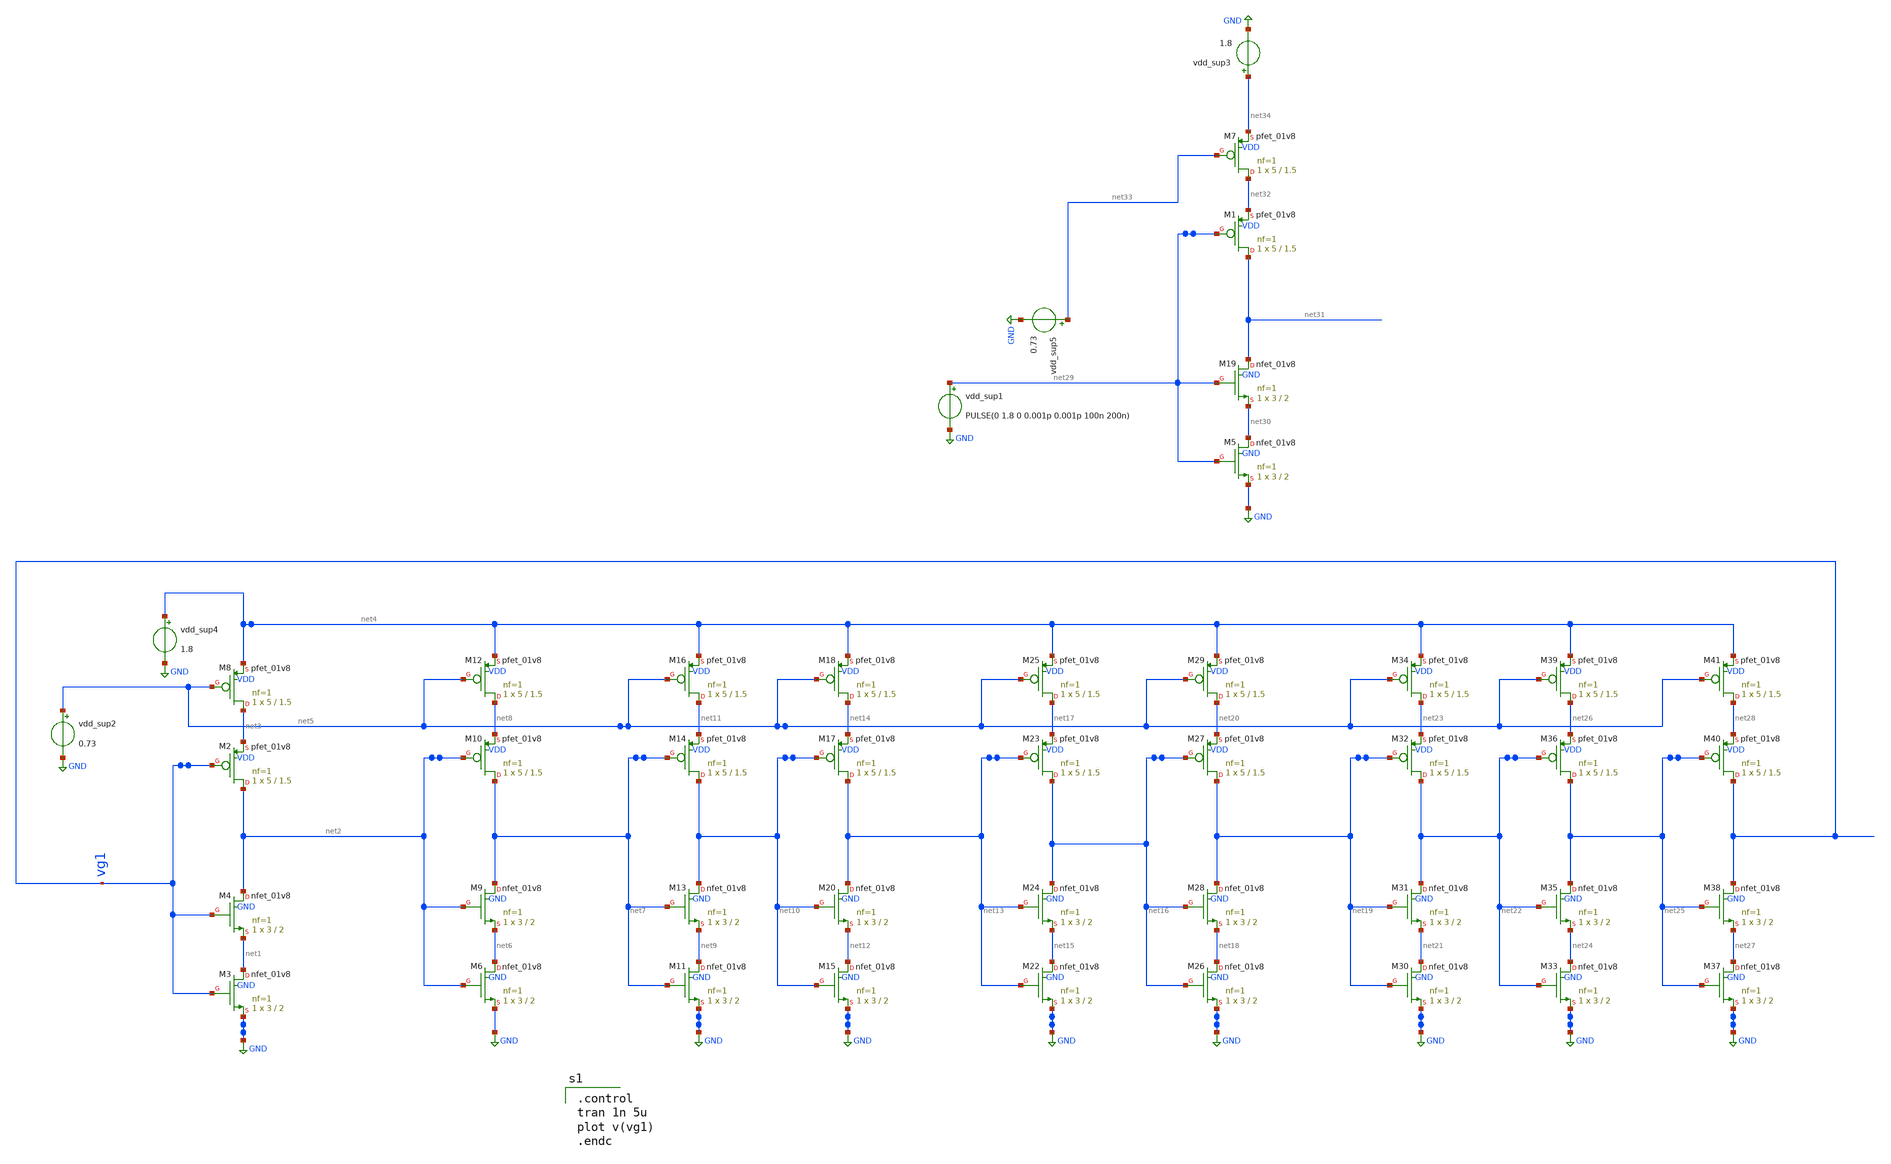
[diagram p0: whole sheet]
** sch_path: ring_osc_28_09.sch
**.subckt ring_osc_28_09
XM2 net2 vg1 net3 VDD sky130_fd_pr__pfet_01v8 L=1.5 W=5 nf=1 ad='int((nf+1)/2) * W/nf * 0.29' as='int((nf+2)/2) * W/nf * 0.29'
+ pd='2*int((nf+1)/2) * (W/nf + 0.29)' ps='2*int((nf+2)/2) * (W/nf + 0.29)' nrd='0.29 / W' nrs='0.29 / W'
+ sa=0 sb=0 sd=0 mult=1 m=1
XM3 net1 vg1 GND GND sky130_fd_pr__nfet_01v8 L=2 W=3 nf=1 ad='int((nf+1)/2) * W/nf * 0.29' as='int((nf+2)/2) * W/nf * 0.29'
+ pd='2*int((nf+1)/2) * (W/nf + 0.29)' ps='2*int((nf+2)/2) * (W/nf + 0.29)' nrd='0.29 / W' nrs='0.29 / W'
+ sa=0 sb=0 sd=0 mult=1 m=1
XM8 net3 net5 net4 VDD sky130_fd_pr__pfet_01v8 L=1.5 W=5 nf=1 ad='int((nf+1)/2) * W/nf * 0.29' as='int((nf+2)/2) * W/nf * 0.29'
+ pd='2*int((nf+1)/2) * (W/nf + 0.29)' ps='2*int((nf+2)/2) * (W/nf + 0.29)' nrd='0.29 / W' nrs='0.29 / W'
+ sa=0 sb=0 sd=0 mult=1 m=1
XM4 net2 vg1 net1 GND sky130_fd_pr__nfet_01v8 L=2 W=3 nf=1 ad='int((nf+1)/2) * W/nf * 0.29' as='int((nf+2)/2) * W/nf * 0.29'
+ pd='2*int((nf+1)/2) * (W/nf + 0.29)' ps='2*int((nf+2)/2) * (W/nf + 0.29)' nrd='0.29 / W' nrs='0.29 / W'
+ sa=0 sb=0 sd=0 mult=1 m=1
vdd_sup2 net5 GND 0.73
XM10 net7 net2 net8 VDD sky130_fd_pr__pfet_01v8 L=1.5 W=5 nf=1 ad='int((nf+1)/2) * W/nf * 0.29' as='int((nf+2)/2) * W/nf * 0.29'
+ pd='2*int((nf+1)/2) * (W/nf + 0.29)' ps='2*int((nf+2)/2) * (W/nf + 0.29)' nrd='0.29 / W' nrs='0.29 / W'
+ sa=0 sb=0 sd=0 mult=1 m=1
XM6 net6 net2 GND GND sky130_fd_pr__nfet_01v8 L=2 W=3 nf=1 ad='int((nf+1)/2) * W/nf * 0.29' as='int((nf+2)/2) * W/nf * 0.29'
+ pd='2*int((nf+1)/2) * (W/nf + 0.29)' ps='2*int((nf+2)/2) * (W/nf + 0.29)' nrd='0.29 / W' nrs='0.29 / W'
+ sa=0 sb=0 sd=0 mult=1 m=1
XM12 net8 net5 net4 VDD sky130_fd_pr__pfet_01v8 L=1.5 W=5 nf=1 ad='int((nf+1)/2) * W/nf * 0.29' as='int((nf+2)/2) * W/nf * 0.29'
+ pd='2*int((nf+1)/2) * (W/nf + 0.29)' ps='2*int((nf+2)/2) * (W/nf + 0.29)' nrd='0.29 / W' nrs='0.29 / W'
+ sa=0 sb=0 sd=0 mult=1 m=1
XM9 net7 net2 net6 GND sky130_fd_pr__nfet_01v8 L=2 W=3 nf=1 ad='int((nf+1)/2) * W/nf * 0.29' as='int((nf+2)/2) * W/nf * 0.29'
+ pd='2*int((nf+1)/2) * (W/nf + 0.29)' ps='2*int((nf+2)/2) * (W/nf + 0.29)' nrd='0.29 / W' nrs='0.29 / W'
+ sa=0 sb=0 sd=0 mult=1 m=1
XM14 net10 net7 net11 VDD sky130_fd_pr__pfet_01v8 L=1.5 W=5 nf=1 ad='int((nf+1)/2) * W/nf * 0.29' as='int((nf+2)/2) * W/nf * 0.29'
+ pd='2*int((nf+1)/2) * (W/nf + 0.29)' ps='2*int((nf+2)/2) * (W/nf + 0.29)' nrd='0.29 / W' nrs='0.29 / W'
+ sa=0 sb=0 sd=0 mult=1 m=1
XM11 net9 net7 GND GND sky130_fd_pr__nfet_01v8 L=2 W=3 nf=1 ad='int((nf+1)/2) * W/nf * 0.29' as='int((nf+2)/2) * W/nf * 0.29'
+ pd='2*int((nf+1)/2) * (W/nf + 0.29)' ps='2*int((nf+2)/2) * (W/nf + 0.29)' nrd='0.29 / W' nrs='0.29 / W'
+ sa=0 sb=0 sd=0 mult=1 m=1
XM16 net11 net5 net4 VDD sky130_fd_pr__pfet_01v8 L=1.5 W=5 nf=1 ad='int((nf+1)/2) * W/nf * 0.29' as='int((nf+2)/2) * W/nf * 0.29'
+ pd='2*int((nf+1)/2) * (W/nf + 0.29)' ps='2*int((nf+2)/2) * (W/nf + 0.29)' nrd='0.29 / W' nrs='0.29 / W'
+ sa=0 sb=0 sd=0 mult=1 m=1
XM13 net10 net7 net9 GND sky130_fd_pr__nfet_01v8 L=2 W=3 nf=1 ad='int((nf+1)/2) * W/nf * 0.29' as='int((nf+2)/2) * W/nf * 0.29'
+ pd='2*int((nf+1)/2) * (W/nf + 0.29)' ps='2*int((nf+2)/2) * (W/nf + 0.29)' nrd='0.29 / W' nrs='0.29 / W'
+ sa=0 sb=0 sd=0 mult=1 m=1
vdd_sup4 net4 GND 1.8
XM17 net13 net10 net14 VDD sky130_fd_pr__pfet_01v8 L=1.5 W=5 nf=1 ad='int((nf+1)/2) * W/nf * 0.29' as='int((nf+2)/2) * W/nf * 0.29'
+ pd='2*int((nf+1)/2) * (W/nf + 0.29)' ps='2*int((nf+2)/2) * (W/nf + 0.29)' nrd='0.29 / W' nrs='0.29 / W'
+ sa=0 sb=0 sd=0 mult=1 m=1
XM15 net12 net10 GND GND sky130_fd_pr__nfet_01v8 L=2 W=3 nf=1 ad='int((nf+1)/2) * W/nf * 0.29' as='int((nf+2)/2) * W/nf * 0.29'
+ pd='2*int((nf+1)/2) * (W/nf + 0.29)' ps='2*int((nf+2)/2) * (W/nf + 0.29)' nrd='0.29 / W' nrs='0.29 / W'
+ sa=0 sb=0 sd=0 mult=1 m=1
XM18 net14 net5 net4 VDD sky130_fd_pr__pfet_01v8 L=1.5 W=5 nf=1 ad='int((nf+1)/2) * W/nf * 0.29' as='int((nf+2)/2) * W/nf * 0.29'
+ pd='2*int((nf+1)/2) * (W/nf + 0.29)' ps='2*int((nf+2)/2) * (W/nf + 0.29)' nrd='0.29 / W' nrs='0.29 / W'
+ sa=0 sb=0 sd=0 mult=1 m=1
XM20 net13 net10 net12 GND sky130_fd_pr__nfet_01v8 L=2 W=3 nf=1 ad='int((nf+1)/2) * W/nf * 0.29' as='int((nf+2)/2) * W/nf * 0.29'
+ pd='2*int((nf+1)/2) * (W/nf + 0.29)' ps='2*int((nf+2)/2) * (W/nf + 0.29)' nrd='0.29 / W' nrs='0.29 / W'
+ sa=0 sb=0 sd=0 mult=1 m=1
XM23 net16 net13 net17 VDD sky130_fd_pr__pfet_01v8 L=1.5 W=5 nf=1 ad='int((nf+1)/2) * W/nf * 0.29' as='int((nf+2)/2) * W/nf * 0.29'
+ pd='2*int((nf+1)/2) * (W/nf + 0.29)' ps='2*int((nf+2)/2) * (W/nf + 0.29)' nrd='0.29 / W' nrs='0.29 / W'
+ sa=0 sb=0 sd=0 mult=1 m=1
XM22 net15 net13 GND GND sky130_fd_pr__nfet_01v8 L=2 W=3 nf=1 ad='int((nf+1)/2) * W/nf * 0.29' as='int((nf+2)/2) * W/nf * 0.29'
+ pd='2*int((nf+1)/2) * (W/nf + 0.29)' ps='2*int((nf+2)/2) * (W/nf + 0.29)' nrd='0.29 / W' nrs='0.29 / W'
+ sa=0 sb=0 sd=0 mult=1 m=1
XM25 net17 net5 net4 VDD sky130_fd_pr__pfet_01v8 L=1.5 W=5 nf=1 ad='int((nf+1)/2) * W/nf * 0.29' as='int((nf+2)/2) * W/nf * 0.29'
+ pd='2*int((nf+1)/2) * (W/nf + 0.29)' ps='2*int((nf+2)/2) * (W/nf + 0.29)' nrd='0.29 / W' nrs='0.29 / W'
+ sa=0 sb=0 sd=0 mult=1 m=1
XM24 net16 net13 net15 GND sky130_fd_pr__nfet_01v8 L=2 W=3 nf=1 ad='int((nf+1)/2) * W/nf * 0.29' as='int((nf+2)/2) * W/nf * 0.29'
+ pd='2*int((nf+1)/2) * (W/nf + 0.29)' ps='2*int((nf+2)/2) * (W/nf + 0.29)' nrd='0.29 / W' nrs='0.29 / W'
+ sa=0 sb=0 sd=0 mult=1 m=1
XM27 net19 net16 net20 VDD sky130_fd_pr__pfet_01v8 L=1.5 W=5 nf=1 ad='int((nf+1)/2) * W/nf * 0.29' as='int((nf+2)/2) * W/nf * 0.29'
+ pd='2*int((nf+1)/2) * (W/nf + 0.29)' ps='2*int((nf+2)/2) * (W/nf + 0.29)' nrd='0.29 / W' nrs='0.29 / W'
+ sa=0 sb=0 sd=0 mult=1 m=1
XM26 net18 net16 GND GND sky130_fd_pr__nfet_01v8 L=2 W=3 nf=1 ad='int((nf+1)/2) * W/nf * 0.29' as='int((nf+2)/2) * W/nf * 0.29'
+ pd='2*int((nf+1)/2) * (W/nf + 0.29)' ps='2*int((nf+2)/2) * (W/nf + 0.29)' nrd='0.29 / W' nrs='0.29 / W'
+ sa=0 sb=0 sd=0 mult=1 m=1
XM29 net20 net5 net4 VDD sky130_fd_pr__pfet_01v8 L=1.5 W=5 nf=1 ad='int((nf+1)/2) * W/nf * 0.29' as='int((nf+2)/2) * W/nf * 0.29'
+ pd='2*int((nf+1)/2) * (W/nf + 0.29)' ps='2*int((nf+2)/2) * (W/nf + 0.29)' nrd='0.29 / W' nrs='0.29 / W'
+ sa=0 sb=0 sd=0 mult=1 m=1
XM28 net19 net16 net18 GND sky130_fd_pr__nfet_01v8 L=2 W=3 nf=1 ad='int((nf+1)/2) * W/nf * 0.29' as='int((nf+2)/2) * W/nf * 0.29'
+ pd='2*int((nf+1)/2) * (W/nf + 0.29)' ps='2*int((nf+2)/2) * (W/nf + 0.29)' nrd='0.29 / W' nrs='0.29 / W'
+ sa=0 sb=0 sd=0 mult=1 m=1
XM32 net22 net19 net23 VDD sky130_fd_pr__pfet_01v8 L=1.5 W=5 nf=1 ad='int((nf+1)/2) * W/nf * 0.29' as='int((nf+2)/2) * W/nf * 0.29'
+ pd='2*int((nf+1)/2) * (W/nf + 0.29)' ps='2*int((nf+2)/2) * (W/nf + 0.29)' nrd='0.29 / W' nrs='0.29 / W'
+ sa=0 sb=0 sd=0 mult=1 m=1
XM30 net21 net19 GND GND sky130_fd_pr__nfet_01v8 L=2 W=3 nf=1 ad='int((nf+1)/2) * W/nf * 0.29' as='int((nf+2)/2) * W/nf * 0.29'
+ pd='2*int((nf+1)/2) * (W/nf + 0.29)' ps='2*int((nf+2)/2) * (W/nf + 0.29)' nrd='0.29 / W' nrs='0.29 / W'
+ sa=0 sb=0 sd=0 mult=1 m=1
XM34 net23 net5 net4 VDD sky130_fd_pr__pfet_01v8 L=1.5 W=5 nf=1 ad='int((nf+1)/2) * W/nf * 0.29' as='int((nf+2)/2) * W/nf * 0.29'
+ pd='2*int((nf+1)/2) * (W/nf + 0.29)' ps='2*int((nf+2)/2) * (W/nf + 0.29)' nrd='0.29 / W' nrs='0.29 / W'
+ sa=0 sb=0 sd=0 mult=1 m=1
XM31 net22 net19 net21 GND sky130_fd_pr__nfet_01v8 L=2 W=3 nf=1 ad='int((nf+1)/2) * W/nf * 0.29' as='int((nf+2)/2) * W/nf * 0.29'
+ pd='2*int((nf+1)/2) * (W/nf + 0.29)' ps='2*int((nf+2)/2) * (W/nf + 0.29)' nrd='0.29 / W' nrs='0.29 / W'
+ sa=0 sb=0 sd=0 mult=1 m=1
XM36 net25 net22 net26 VDD sky130_fd_pr__pfet_01v8 L=1.5 W=5 nf=1 ad='int((nf+1)/2) * W/nf * 0.29' as='int((nf+2)/2) * W/nf * 0.29'
+ pd='2*int((nf+1)/2) * (W/nf + 0.29)' ps='2*int((nf+2)/2) * (W/nf + 0.29)' nrd='0.29 / W' nrs='0.29 / W'
+ sa=0 sb=0 sd=0 mult=1 m=1
XM33 net24 net22 GND GND sky130_fd_pr__nfet_01v8 L=2 W=3 nf=1 ad='int((nf+1)/2) * W/nf * 0.29' as='int((nf+2)/2) * W/nf * 0.29'
+ pd='2*int((nf+1)/2) * (W/nf + 0.29)' ps='2*int((nf+2)/2) * (W/nf + 0.29)' nrd='0.29 / W' nrs='0.29 / W'
+ sa=0 sb=0 sd=0 mult=1 m=1
XM39 net26 net5 net4 VDD sky130_fd_pr__pfet_01v8 L=1.5 W=5 nf=1 ad='int((nf+1)/2) * W/nf * 0.29' as='int((nf+2)/2) * W/nf * 0.29'
+ pd='2*int((nf+1)/2) * (W/nf + 0.29)' ps='2*int((nf+2)/2) * (W/nf + 0.29)' nrd='0.29 / W' nrs='0.29 / W'
+ sa=0 sb=0 sd=0 mult=1 m=1
XM35 net25 net22 net24 GND sky130_fd_pr__nfet_01v8 L=2 W=3 nf=1 ad='int((nf+1)/2) * W/nf * 0.29' as='int((nf+2)/2) * W/nf * 0.29'
+ pd='2*int((nf+1)/2) * (W/nf + 0.29)' ps='2*int((nf+2)/2) * (W/nf + 0.29)' nrd='0.29 / W' nrs='0.29 / W'
+ sa=0 sb=0 sd=0 mult=1 m=1
XM40 vg1 net25 net28 VDD sky130_fd_pr__pfet_01v8 L=1.5 W=5 nf=1 ad='int((nf+1)/2) * W/nf * 0.29' as='int((nf+2)/2) * W/nf * 0.29'
+ pd='2*int((nf+1)/2) * (W/nf + 0.29)' ps='2*int((nf+2)/2) * (W/nf + 0.29)' nrd='0.29 / W' nrs='0.29 / W'
+ sa=0 sb=0 sd=0 mult=1 m=1
XM37 net27 net25 GND GND sky130_fd_pr__nfet_01v8 L=2 W=3 nf=1 ad='int((nf+1)/2) * W/nf * 0.29' as='int((nf+2)/2) * W/nf * 0.29'
+ pd='2*int((nf+1)/2) * (W/nf + 0.29)' ps='2*int((nf+2)/2) * (W/nf + 0.29)' nrd='0.29 / W' nrs='0.29 / W'
+ sa=0 sb=0 sd=0 mult=1 m=1
XM41 net28 net5 net4 VDD sky130_fd_pr__pfet_01v8 L=1.5 W=5 nf=1 ad='int((nf+1)/2) * W/nf * 0.29' as='int((nf+2)/2) * W/nf * 0.29'
+ pd='2*int((nf+1)/2) * (W/nf + 0.29)' ps='2*int((nf+2)/2) * (W/nf + 0.29)' nrd='0.29 / W' nrs='0.29 / W'
+ sa=0 sb=0 sd=0 mult=1 m=1
XM38 vg1 net25 net27 GND sky130_fd_pr__nfet_01v8 L=2 W=3 nf=1 ad='int((nf+1)/2) * W/nf * 0.29' as='int((nf+2)/2) * W/nf * 0.29'
+ pd='2*int((nf+1)/2) * (W/nf + 0.29)' ps='2*int((nf+2)/2) * (W/nf + 0.29)' nrd='0.29 / W' nrs='0.29 / W'
+ sa=0 sb=0 sd=0 mult=1 m=1
XM1 net31 net29 net32 VDD sky130_fd_pr__pfet_01v8 L=1.5 W=5 nf=1 ad='int((nf+1)/2) * W/nf * 0.29' as='int((nf+2)/2) * W/nf * 0.29'
+ pd='2*int((nf+1)/2) * (W/nf + 0.29)' ps='2*int((nf+2)/2) * (W/nf + 0.29)' nrd='0.29 / W' nrs='0.29 / W'
+ sa=0 sb=0 sd=0 mult=1 m=1
XM5 net30 net29 GND GND sky130_fd_pr__nfet_01v8 L=2 W=3 nf=1 ad='int((nf+1)/2) * W/nf * 0.29' as='int((nf+2)/2) * W/nf * 0.29'
+ pd='2*int((nf+1)/2) * (W/nf + 0.29)' ps='2*int((nf+2)/2) * (W/nf + 0.29)' nrd='0.29 / W' nrs='0.29 / W'
+ sa=0 sb=0 sd=0 mult=1 m=1
XM7 net32 net33 net34 VDD sky130_fd_pr__pfet_01v8 L=1.5 W=5 nf=1 ad='int((nf+1)/2) * W/nf * 0.29' as='int((nf+2)/2) * W/nf * 0.29'
+ pd='2*int((nf+1)/2) * (W/nf + 0.29)' ps='2*int((nf+2)/2) * (W/nf + 0.29)' nrd='0.29 / W' nrs='0.29 / W'
+ sa=0 sb=0 sd=0 mult=1 m=1
XM19 net31 net29 net30 GND sky130_fd_pr__nfet_01v8 L=2 W=3 nf=1 ad='int((nf+1)/2) * W/nf * 0.29' as='int((nf+2)/2) * W/nf * 0.29'
+ pd='2*int((nf+1)/2) * (W/nf + 0.29)' ps='2*int((nf+2)/2) * (W/nf + 0.29)' nrd='0.29 / W' nrs='0.29 / W'
+ sa=0 sb=0 sd=0 mult=1 m=1
vdd_sup1 net29 GND PULSE(0 1.8 0 0.001p 0.001p 100n 200n)
vdd_sup3 net34 GND 1.8
vdd_sup5 net33 GND 0.73
**** begin user architecture code


.lib /home/cegrahul/open_pdks/sky130/sky130A/libs.tech/ngspice/sky130.lib.spice tt
.MODEL swmod SW(VT=0.0 VH=0.01 RON=1 ROFF=10000000000)


.control
tran 1n 5u
plot v(vg1)
.endc

**** end user architecture code
**.ends
.GLOBAL GND
.end
